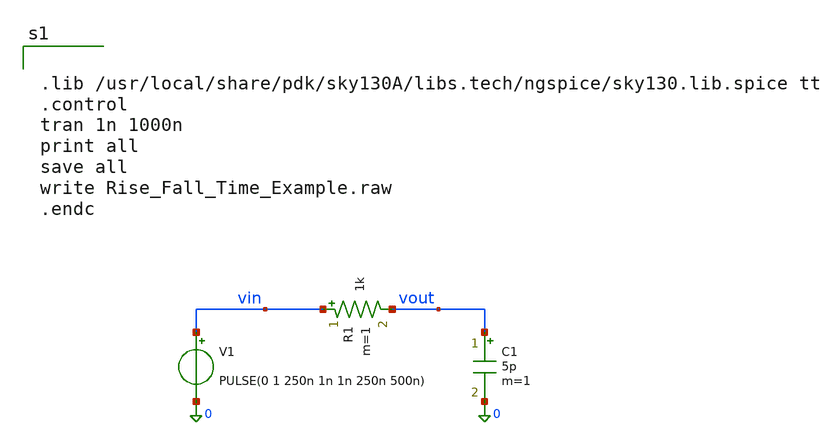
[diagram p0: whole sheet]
** sch_path: mag/Rise_Fall_Time_Example.sch
**.subckt Rise_Fall_Time_Example
V1 vin 0 PULSE(0 1 250n 1n 1n 250n 500n)
R1 vin vout 1k m=1
C1 vout 0 5p m=1
**** begin user architecture code


.lib /usr/local/share/pdk/sky130A/libs.tech/ngspice/sky130.lib.spice tt
.control
tran 1n 1000n
print all
save all
write Rise_Fall_Time_Example.raw
.endc

**** end user architecture code
**.ends
.end
